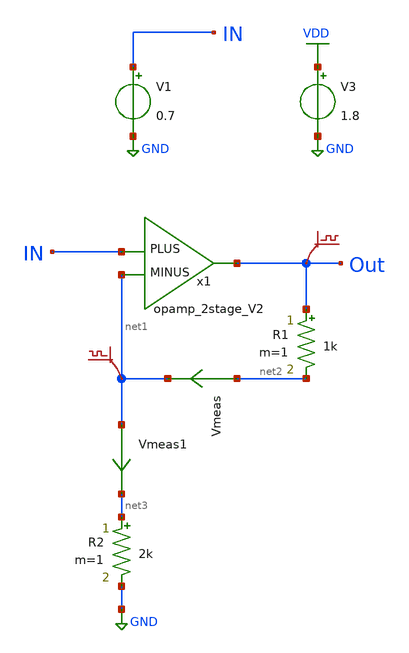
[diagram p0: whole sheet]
** sch_path: lib/xschem/LDO/test_opamp_V2.sch
**.subckt test_opamp_V2
R1 Out net2 1k m=1
V1 IN GND 0.7
V3 VDD GND 1.8
R2 net3 GND 2k m=1
Vmeas net2 net1 0
.save i(vmeas)
Vmeas1 net1 net3 0
.save i(vmeas1)
x1 net1 IN Out VDD GND opamp_2stage_V2
.save v(out)
.save v(net1)
**** begin user architecture code

.lib $::SKYWATER_MODELS/sky130.lib.spice tt


**** end user architecture code
**.ends

* expanding   symbol:  LDO/opamp_2stage_V2.sym # of pins=3
** sym_path: lib/xschem/LDO/opamp_2stage_V2.sym
** sch_path: lib/xschem/LDO/opamp_2stage_V2.sch
.subckt opamp_2stage_V2 MINUS PLUS Vout VDD GND
*.ipin PLUS
*.ipin MINUS
*.opin Vout
C3 net6 Vout 2p m=1
XM6 net3 net3 GND GND sky130_fd_pr__nfet_01v8 L=0.15 W=2 nf=1 ad='int((nf+1)/2) * W/nf * 0.29' as='int((nf+2)/2) * W/nf * 0.29'
+ pd='2*int((nf+1)/2) * (W/nf + 0.29)' ps='2*int((nf+2)/2) * (W/nf + 0.29)' nrd='0.29 / W' nrs='0.29 / W'
+ sa=0 sb=0 sd=0 mult=1 m=1
XM5 net5 net3 GND GND sky130_fd_pr__nfet_01v8 L=0.15 W=2 nf=1 ad='int((nf+1)/2) * W/nf * 0.29' as='int((nf+2)/2) * W/nf * 0.29'
+ pd='2*int((nf+1)/2) * (W/nf + 0.29)' ps='2*int((nf+2)/2) * (W/nf + 0.29)' nrd='0.29 / W' nrs='0.29 / W'
+ sa=0 sb=0 sd=0 mult=1 m=1
XM7 net2 PLUS net1 VDD sky130_fd_pr__pfet_01v8 L=0.15 W=5 nf=1 ad='int((nf+1)/2) * W/nf * 0.29' as='int((nf+2)/2) * W/nf * 0.29'
+ pd='2*int((nf+1)/2) * (W/nf + 0.29)' ps='2*int((nf+2)/2) * (W/nf + 0.29)' nrd='0.29 / W' nrs='0.29 / W'
+ sa=0 sb=0 sd=0 mult=1 m=1
XM10 net4 MINUS net1 VDD sky130_fd_pr__pfet_01v8 L=0.15 W=5 nf=1 ad='int((nf+1)/2) * W/nf * 0.29' as='int((nf+2)/2) * W/nf * 0.29'
+ pd='2*int((nf+1)/2) * (W/nf + 0.29)' ps='2*int((nf+2)/2) * (W/nf + 0.29)' nrd='0.29 / W' nrs='0.29 / W'
+ sa=0 sb=0 sd=0 mult=1 m=1
XM11 net1 Vbias VDD VDD sky130_fd_pr__pfet_01v8 L=0.15 W=5 nf=1 ad='int((nf+1)/2) * W/nf * 0.29' as='int((nf+2)/2) * W/nf * 0.29'
+ pd='2*int((nf+1)/2) * (W/nf + 0.29)' ps='2*int((nf+2)/2) * (W/nf + 0.29)' nrd='0.29 / W' nrs='0.29 / W'
+ sa=0 sb=0 sd=0 mult=1 m=1
XM13 Vout net5 GND GND sky130_fd_pr__nfet_01v8 L=0.15 W=5 nf=1 ad='int((nf+1)/2) * W/nf * 0.29' as='int((nf+2)/2) * W/nf * 0.29'
+ pd='2*int((nf+1)/2) * (W/nf + 0.29)' ps='2*int((nf+2)/2) * (W/nf + 0.29)' nrd='0.29 / W' nrs='0.29 / W'
+ sa=0 sb=0 sd=0 mult=1 m=1
XM16 net7 Vbias VDD VDD sky130_fd_pr__pfet_01v8 L=0.15 W=5 nf=1 ad='int((nf+1)/2) * W/nf * 0.29' as='int((nf+2)/2) * W/nf * 0.29'
+ pd='2*int((nf+1)/2) * (W/nf + 0.29)' ps='2*int((nf+2)/2) * (W/nf + 0.29)' nrd='0.29 / W' nrs='0.29 / W'
+ sa=0 sb=0 sd=0 mult=1 m=1
.save v(plus)
.save v(minus)
.save v(net2)
.save v(net4)
.save v(minus)
.save v(vout)
.save v(plus)
Vmeas1 net4 net3 0
.save i(vmeas1)
Vmeas2 net2 net5 0
.save i(vmeas2)
Vmeas3 net7 Vout 0
.save i(vmeas3)
Vmeas5 net2 net8 0
.save i(vmeas5)
x1 Vbias Vcs VDD GND casc_mirror
XM1 net6 Vcs net8 GND sky130_fd_pr__nfet_01v8 L=0.15 W=1 nf=1 ad='int((nf+1)/2) * W/nf * 0.29' as='int((nf+2)/2) * W/nf * 0.29'
+ pd='2*int((nf+1)/2) * (W/nf + 0.29)' ps='2*int((nf+2)/2) * (W/nf + 0.29)' nrd='0.29 / W' nrs='0.29 / W'
+ sa=0 sb=0 sd=0 mult=1 m=1
.save v(net6)
.save v(vbias)
.save v(vbias)
.ends


* expanding   symbol:  LDO/casc_mirror.sym # of pins=2
** sym_path: lib/xschem/LDO/casc_mirror.sym
** sch_path: lib/xschem/LDO/casc_mirror.sch
.subckt casc_mirror Vbias Vcs VDD GND
*.opin Vbias
*.opin Vcs
XM8 Vbias Vbias net3 VDD sky130_fd_pr__pfet_01v8 L=0.15 W=2 nf=1 ad='int((nf+1)/2) * W/nf * 0.29' as='int((nf+2)/2) * W/nf * 0.29'
+ pd='2*int((nf+1)/2) * (W/nf + 0.29)' ps='2*int((nf+2)/2) * (W/nf + 0.29)' nrd='0.29 / W' nrs='0.29 / W'
+ sa=0 sb=0 sd=0 mult=1 m=1
XM9 net7 net1 net4 GND sky130_fd_pr__nfet_01v8 L=0.15 W=7 nf=1 ad='int((nf+1)/2) * W/nf * 0.29' as='int((nf+2)/2) * W/nf * 0.29'
+ pd='2*int((nf+1)/2) * (W/nf + 0.29)' ps='2*int((nf+2)/2) * (W/nf + 0.29)' nrd='0.29 / W' nrs='0.29 / W'
+ sa=0 sb=0 sd=0 mult=1 m=1
XM1 Vcs Vbias net3 VDD sky130_fd_pr__pfet_01v8 L=0.15 W=2 nf=1 ad='int((nf+1)/2) * W/nf * 0.29' as='int((nf+2)/2) * W/nf * 0.29'
+ pd='2*int((nf+1)/2) * (W/nf + 0.29)' ps='2*int((nf+2)/2) * (W/nf + 0.29)' nrd='0.29 / W' nrs='0.29 / W'
+ sa=0 sb=0 sd=0 mult=1 m=1
XM2 net9 net2 net8 GND sky130_fd_pr__nfet_01v8 L=0.15 W=2 nf=1 ad='int((nf+1)/2) * W/nf * 0.29' as='int((nf+2)/2) * W/nf * 0.29'
+ pd='2*int((nf+1)/2) * (W/nf + 0.29)' ps='2*int((nf+2)/2) * (W/nf + 0.29)' nrd='0.29 / W' nrs='0.29 / W'
+ sa=0 sb=0 sd=0 mult=1 m=1
XM3 net2 net2 net6 GND sky130_fd_pr__nfet_01v8 L=0.15 W=2 nf=1 ad='int((nf+1)/2) * W/nf * 0.29' as='int((nf+2)/2) * W/nf * 0.29'
+ pd='2*int((nf+1)/2) * (W/nf + 0.29)' ps='2*int((nf+2)/2) * (W/nf + 0.29)' nrd='0.29 / W' nrs='0.29 / W'
+ sa=0 sb=0 sd=0 mult=1 m=1
XM4 net1 net1 GND GND sky130_fd_pr__nfet_01v8 L=0.15 W=2 nf=1 ad='int((nf+1)/2) * W/nf * 0.29' as='int((nf+2)/2) * W/nf * 0.29'
+ pd='2*int((nf+1)/2) * (W/nf + 0.29)' ps='2*int((nf+2)/2) * (W/nf + 0.29)' nrd='0.29 / W' nrs='0.29 / W'
+ sa=0 sb=0 sd=0 mult=1 m=1
R1 net5 GND 1k m=1
Vmeas_ref2 net4 net5 0
.save i(vmeas_ref2)
Vmeas1 net6 net1 0
.save i(vmeas1)
Vmeas_ref1 net8 net7 0
.save i(vmeas_ref1)
.save v(net7)
.save v(net5)
.save v(net1)
Vmeas_ref3 Vbias net9 0
.save i(vmeas_ref3)
Vmeas_ref4 Vcs net2 0
.save i(vmeas_ref4)
Vmeas_ref5 VDD net10 0
.save i(vmeas_ref5)
I0 net10 net3 0.25u
.save v(vbias)
.save v(vcs)
.ends

.GLOBAL GND
.GLOBAL VDD
**** begin user architecture code


.control
save all
op
write test_opamp_V2.raw
.endc


**** end user architecture code
.end
